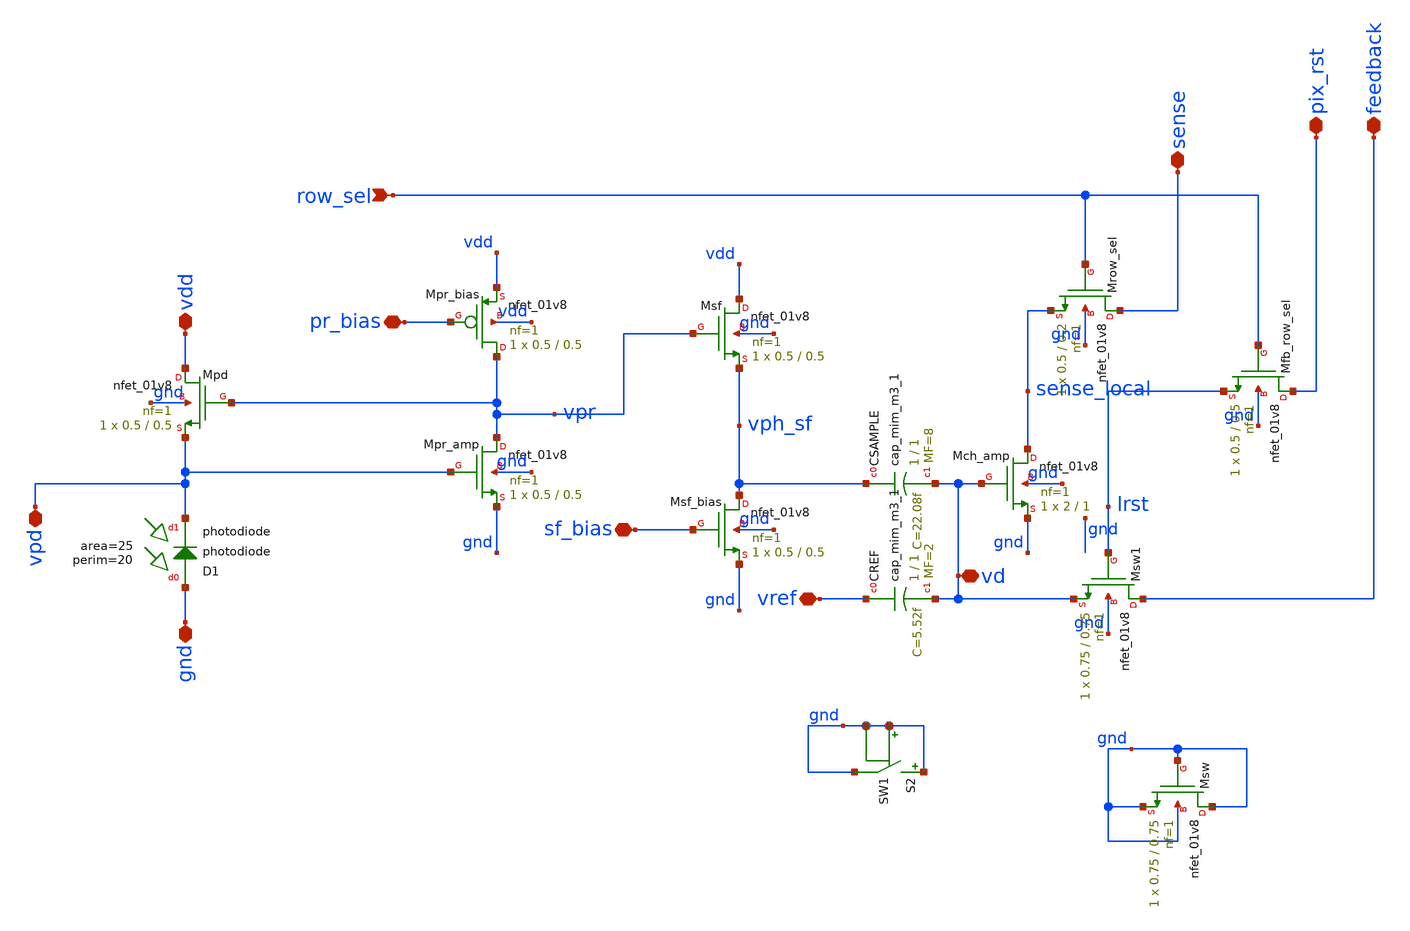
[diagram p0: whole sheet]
** sch_path: analog/xschem/col_amp_n_clamp_v1/openDVS_pixel_tia_RL_v1.sch
**.subckt openDVS_pixel_tia_RL_v1 row_sel sense pix_rst feedback pr_bias vdd vref vpd sf_bias gnd vd
*.ipin row_sel
*.iopin sense
*.iopin pix_rst
*.iopin feedback
*.iopin pr_bias
*.iopin vdd
*.iopin vref
*.iopin vpd
*.iopin sf_bias
*.iopin gnd
*.iopin vd
XCSAMPLE vph_sf vd sky130_fd_pr__cap_mim_m3_1 W=1 L=1 MF=8 m=8
XCREF vref vd sky130_fd_pr__cap_mim_m3_1 W=1 L=1 MF=2 m=2
XMpd vdd vpr vpd gnd sky130_fd_pr__nfet_01v8 L=0.5 W=0.5 nf=1 ad='int((1 + 1)/2) * 0.5 / 1 * 0.29' as='int((1 + 2)/2) * 0.5 / 1 * 0.29'
+ pd='2*int((1 + 1)/2) * (0.5 / 1 + 0.29)' ps='2*int((1 + 2)/2) * (0.5 / 1 + 0.29)' nrd='0.29 / 0.5 ' nrs='0.29 / 0.5 '
+ sa=0 sb=0 sd=0 mult=1 m=1
XMch_amp sense_local vd gnd gnd sky130_fd_pr__nfet_01v8 L=1 W=2 nf=1 ad='int((1 + 1)/2) * 2 / 1 * 0.29'
+ as='int((1 + 2)/2) * 2 / 1 * 0.29' pd='2*int((1 + 1)/2) * (2 / 1 + 0.29)' ps='2*int((1 + 2)/2) * (2 / 1 + 0.29)'
+ nrd='0.29 / 2 ' nrs='0.29 / 2 ' sa=0 sb=0 sd=0 mult=1 m=1
XMsw gnd gnd gnd gnd sky130_fd_pr__nfet_01v8 L=0.75 W=0.75 nf=1 ad='int((1 + 1)/2) * 0.75 / 1 * 0.29'
+ as='int((1 + 2)/2) * 0.75 / 1 * 0.29' pd='2*int((1 + 1)/2) * (0.75 / 1 + 0.29)' ps='2*int((1 + 2)/2) * (0.75 / 1 + 0.29)'
+ nrd='0.29 / 0.75 ' nrs='0.29 / 0.75 ' sa=0 sb=0 sd=0 mult=1 m=1
XMsf_bias vph_sf sf_bias gnd gnd sky130_fd_pr__nfet_01v8 L=0.5 W=0.5 nf=1 ad='int((1 + 1)/2) * 0.5 / 1 * 0.29'
+ as='int((1 + 2)/2) * 0.5 / 1 * 0.29' pd='2*int((1 + 1)/2) * (0.5 / 1 + 0.29)' ps='2*int((1 + 2)/2) * (0.5 / 1 + 0.29)'
+ nrd='0.29 / 0.5 ' nrs='0.29 / 0.5 ' sa=0 sb=0 sd=0 mult=1 m=1
XMsf vdd vpr vph_sf gnd sky130_fd_pr__nfet_01v8 L=0.5 W=0.5 nf=1 ad='int((1 + 1)/2) * 0.5 / 1 * 0.29'
+ as='int((1 + 2)/2) * 0.5 / 1 * 0.29' pd='2*int((1 + 1)/2) * (0.5 / 1 + 0.29)' ps='2*int((1 + 2)/2) * (0.5 / 1 + 0.29)'
+ nrd='0.29 / 0.5 ' nrs='0.29 / 0.5 ' sa=0 sb=0 sd=0 mult=1 m=1
XMrow_sel sense row_sel sense_local gnd sky130_fd_pr__nfet_01v8 L=0.2 W=0.5 nf=1 ad='int((1 + 1)/2) * 0.5 / 1 * 0.29'
+ as='int((1 + 2)/2) * 0.5 / 1 * 0.29' pd='2*int((1 + 1)/2) * (0.5 / 1 + 0.29)' ps='2*int((1 + 2)/2) * (0.5 / 1 + 0.29)'
+ nrd='0.29 / 0.5 ' nrs='0.29 / 0.5 ' sa=0 sb=0 sd=0 mult=1 m=1
XMfb_row_sel pix_rst row_sel lrst gnd sky130_fd_pr__nfet_01v8 L=0.5 W=0.5 nf=1 ad='int((1 + 1)/2) * 0.5 / 1 * 0.29'
+ as='int((1 + 2)/2) * 0.5 / 1 * 0.29' pd='2*int((1 + 1)/2) * (0.5 / 1 + 0.29)' ps='2*int((1 + 2)/2) * (0.5 / 1 + 0.29)'
+ nrd='0.29 / 0.5 ' nrs='0.29 / 0.5 ' sa=0 sb=0 sd=0 mult=1 m=1
XMpr_amp vpr vpd gnd gnd sky130_fd_pr__nfet_01v8 L=0.5 W=0.5 nf=1 ad='int((1 + 1)/2) * 0.5 / 1 * 0.29'
+ as='int((1 + 2)/2) * 0.5 / 1 * 0.29' pd='2*int((1 + 1)/2) * (0.5 / 1 + 0.29)' ps='2*int((1 + 2)/2) * (0.5 / 1 + 0.29)'
+ nrd='0.29 / 0.5 ' nrs='0.29 / 0.5 ' sa=0 sb=0 sd=0 mult=1 m=1
XMpr_bias vpr pr_bias vdd vdd sky130_fd_pr__nfet_01v8 L=0.5 W=0.5 nf=1 ad='int((1 + 1)/2) * 0.5 / 1 * 0.29'
+ as='int((1 + 2)/2) * 0.5 / 1 * 0.29' pd='2*int((1 + 1)/2) * (0.5 / 1 + 0.29)' ps='2*int((1 + 2)/2) * (0.5 / 1 + 0.29)'
+ nrd='0.29 / 0.5 ' nrs='0.29 / 0.5 ' sa=0 sb=0 sd=0 mult=1 m=1
XD1 gnd vpd sky130_fd_pr__photodiode area=25 perim=20
S2 gnd gnd gnd gnd SW1
XMsw1 feedback lrst vd gnd sky130_fd_pr__nfet_01v8 L=0.75 W=0.75 nf=1 ad='int((1 + 1)/2) * 0.75 / 1 * 0.29'
+ as='int((1 + 2)/2) * 0.75 / 1 * 0.29' pd='2*int((1 + 1)/2) * (0.75 / 1 + 0.29)' ps='2*int((1 + 2)/2) * (0.75 / 1 + 0.29)'
+ nrd='0.29 / 0.75 ' nrs='0.29 / 0.75 ' sa=0 sb=0 sd=0 mult=1 m=1
**.ends
**** begin user architecture code
.MODEL SW1 SW   VT=0.9 VH=0.01  RON=0.01 ROFF=10G
**** end user architecture code
.end
